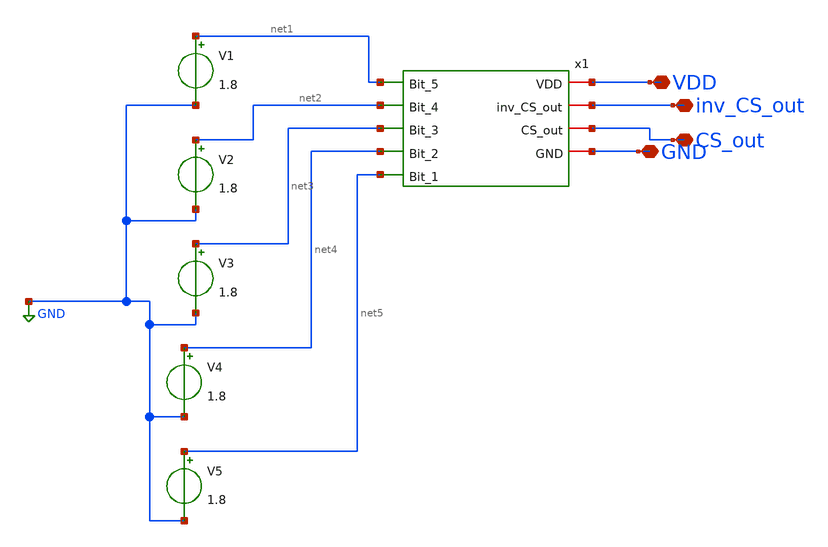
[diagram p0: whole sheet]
** sch_path: ProjectDesigns/5BitAND/Sim_5bitAND_sym.sch
**.subckt Sim_5bitAND_sym inv_CS_out CS_out VDD GND
*.iopin inv_CS_out
*.iopin CS_out
*.iopin VDD
*.iopin GND
V1 net1 GND 1.8
V2 net2 GND 1.8
V3 net3 GND 1.8
V4 net4 GND 1.8
V5 net5 GND 1.8
x1 VDD inv_CS_out net1 net2 CS_out net3 net4 net5 GND 5bit_AND
**.ends

* expanding   symbol:  /home/shalini1234/Project/5bit_AND.sym # of pins=9
** sym_path: ProjectDesigns/5BitAND/5bit_AND.sym
** sch_path: ProjectDesigns/5BitAND/5bit_AND.sch
.subckt 5bit_AND VDD inv_CS_out Bit_5 Bit_4 CS_out Bit_3 Bit_2 Bit_1 GND
*.ipin Bit_1
*.ipin Bit_3
*.ipin Bit_2
*.ipin Bit_4
*.ipin Bit_5
*.iopin inv_CS_out
*.iopin CS_out
*.iopin VDD
*.iopin GND
XM1 inv_CS_out Bit_5 net1 net1 sky130_fd_pr__nfet_01v8 L=0.15 W=1 nf=1 ad='int((nf+1)/2) * W/nf * 0.29'
+ as='int((nf+2)/2) * W/nf * 0.29' pd='2*int((nf+1)/2) * (W/nf + 0.29)' ps='2*int((nf+2)/2) * (W/nf + 0.29)'
+ nrd='0.29 / W' nrs='0.29 / W' sa=0 sb=0 sd=0 mult=1 m=1
XM2 net1 Bit_4 net2 net2 sky130_fd_pr__nfet_01v8 L=0.15 W=1 nf=1 ad='int((nf+1)/2) * W/nf * 0.29' as='int((nf+2)/2) * W/nf * 0.29'
+ pd='2*int((nf+1)/2) * (W/nf + 0.29)' ps='2*int((nf+2)/2) * (W/nf + 0.29)' nrd='0.29 / W' nrs='0.29 / W'
+ sa=0 sb=0 sd=0 mult=1 m=1
XM3 net2 Bit_3 net3 net3 sky130_fd_pr__nfet_01v8 L=0.15 W=1 nf=1 ad='int((nf+1)/2) * W/nf * 0.29' as='int((nf+2)/2) * W/nf * 0.29'
+ pd='2*int((nf+1)/2) * (W/nf + 0.29)' ps='2*int((nf+2)/2) * (W/nf + 0.29)' nrd='0.29 / W' nrs='0.29 / W'
+ sa=0 sb=0 sd=0 mult=1 m=1
XM4 net3 Bit_2 net4 net4 sky130_fd_pr__nfet_01v8 L=0.15 W=1 nf=1 ad='int((nf+1)/2) * W/nf * 0.29' as='int((nf+2)/2) * W/nf * 0.29'
+ pd='2*int((nf+1)/2) * (W/nf + 0.29)' ps='2*int((nf+2)/2) * (W/nf + 0.29)' nrd='0.29 / W' nrs='0.29 / W'
+ sa=0 sb=0 sd=0 mult=1 m=1
XM5 net4 Bit_1 GND GND sky130_fd_pr__nfet_01v8 L=0.15 W=1 nf=1 ad='int((nf+1)/2) * W/nf * 0.29' as='int((nf+2)/2) * W/nf * 0.29'
+ pd='2*int((nf+1)/2) * (W/nf + 0.29)' ps='2*int((nf+2)/2) * (W/nf + 0.29)' nrd='0.29 / W' nrs='0.29 / W'
+ sa=0 sb=0 sd=0 mult=1 m=1
XM6 inv_CS_out Bit_3 VDD VDD sky130_fd_pr__pfet_01v8 L=0.15 W=1 nf=1 ad='int((nf+1)/2) * W/nf * 0.29'
+ as='int((nf+2)/2) * W/nf * 0.29' pd='2*int((nf+1)/2) * (W/nf + 0.29)' ps='2*int((nf+2)/2) * (W/nf + 0.29)'
+ nrd='0.29 / W' nrs='0.29 / W' sa=0 sb=0 sd=0 mult=1 m=1
XM7 inv_CS_out Bit_2 VDD VDD sky130_fd_pr__pfet_01v8 L=0.15 W=1 nf=1 ad='int((nf+1)/2) * W/nf * 0.29'
+ as='int((nf+2)/2) * W/nf * 0.29' pd='2*int((nf+1)/2) * (W/nf + 0.29)' ps='2*int((nf+2)/2) * (W/nf + 0.29)'
+ nrd='0.29 / W' nrs='0.29 / W' sa=0 sb=0 sd=0 mult=1 m=1
XM8 inv_CS_out Bit_1 VDD VDD sky130_fd_pr__pfet_01v8 L=0.15 W=1 nf=1 ad='int((nf+1)/2) * W/nf * 0.29'
+ as='int((nf+2)/2) * W/nf * 0.29' pd='2*int((nf+1)/2) * (W/nf + 0.29)' ps='2*int((nf+2)/2) * (W/nf + 0.29)'
+ nrd='0.29 / W' nrs='0.29 / W' sa=0 sb=0 sd=0 mult=1 m=1
XM9 inv_CS_out Bit_4 VDD VDD sky130_fd_pr__pfet_01v8 L=0.15 W=1 nf=1 ad='int((nf+1)/2) * W/nf * 0.29'
+ as='int((nf+2)/2) * W/nf * 0.29' pd='2*int((nf+1)/2) * (W/nf + 0.29)' ps='2*int((nf+2)/2) * (W/nf + 0.29)'
+ nrd='0.29 / W' nrs='0.29 / W' sa=0 sb=0 sd=0 mult=1 m=1
XM10 inv_CS_out Bit_5 VDD VDD sky130_fd_pr__pfet_01v8 L=0.15 W=1 nf=1 ad='int((nf+1)/2) * W/nf * 0.29'
+ as='int((nf+2)/2) * W/nf * 0.29' pd='2*int((nf+1)/2) * (W/nf + 0.29)' ps='2*int((nf+2)/2) * (W/nf + 0.29)'
+ nrd='0.29 / W' nrs='0.29 / W' sa=0 sb=0 sd=0 mult=1 m=1
XM11 CS_out inv_CS_out GND GND sky130_fd_pr__nfet_01v8 L=0.15 W=1 nf=1 ad='int((nf+1)/2) * W/nf * 0.29'
+ as='int((nf+2)/2) * W/nf * 0.29' pd='2*int((nf+1)/2) * (W/nf + 0.29)' ps='2*int((nf+2)/2) * (W/nf + 0.29)'
+ nrd='0.29 / W' nrs='0.29 / W' sa=0 sb=0 sd=0 mult=1 m=1
XM12 CS_out inv_CS_out VDD VDD sky130_fd_pr__pfet_01v8 L=0.15 W=1 nf=1 ad='int((nf+1)/2) * W/nf * 0.29'
+ as='int((nf+2)/2) * W/nf * 0.29' pd='2*int((nf+1)/2) * (W/nf + 0.29)' ps='2*int((nf+2)/2) * (W/nf + 0.29)'
+ nrd='0.29 / W' nrs='0.29 / W' sa=0 sb=0 sd=0 mult=1 m=1
.ends

.GLOBAL GND
.end
